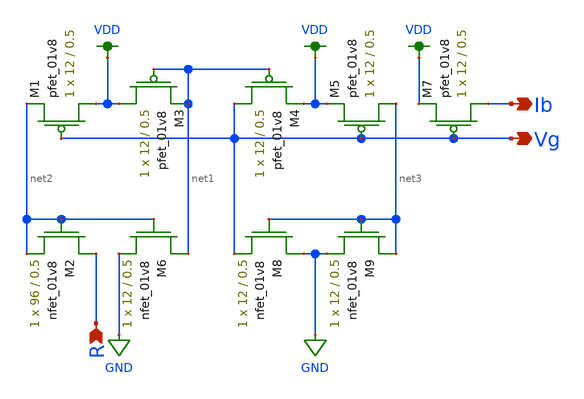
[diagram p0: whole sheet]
** sch_path: bias_gen.sch
**.subckt bias_gen R Ib Vg
*.ipin R
*.opin Ib
*.opin Vg
XM2 R net2 net2 GND sky130_fd_pr__nfet_01v8 L=0.5 W=96 nf=1 ad='int((nf+1)/2) * W/nf * 0.29' as='int((nf+2)/2) * W/nf * 0.29'
+ pd='2*int((nf+1)/2) * (W/nf + 0.29)' ps='2*int((nf+2)/2) * (W/nf + 0.29)' nrd='0.29 / W' nrs='0.29 / W'
+ sa=0 sb=0 sd=0 mult=1 m=1
XM3 VDD net1 net1 VDD sky130_fd_pr__pfet_01v8 L=0.5 W=12 nf=1 ad='int((nf+1)/2) * W/nf * 0.29' as='int((nf+2)/2) * W/nf * 0.29'
+ pd='2*int((nf+1)/2) * (W/nf + 0.29)' ps='2*int((nf+2)/2) * (W/nf + 0.29)' nrd='0.29 / W' nrs='0.29 / W'
+ sa=0 sb=0 sd=0 mult=1 m=1
XM1 VDD Vg net2 VDD sky130_fd_pr__pfet_01v8 L=0.5 W=12 nf=1 ad='int((nf+1)/2) * W/nf * 0.29' as='int((nf+2)/2) * W/nf * 0.29'
+ pd='2*int((nf+1)/2) * (W/nf + 0.29)' ps='2*int((nf+2)/2) * (W/nf + 0.29)' nrd='0.29 / W' nrs='0.29 / W'
+ sa=0 sb=0 sd=0 mult=1 m=1
XM4 Vg net1 VDD VDD sky130_fd_pr__pfet_01v8 L=0.5 W=12 nf=1 ad='int((nf+1)/2) * W/nf * 0.29' as='int((nf+2)/2) * W/nf * 0.29'
+ pd='2*int((nf+1)/2) * (W/nf + 0.29)' ps='2*int((nf+2)/2) * (W/nf + 0.29)' nrd='0.29 / W' nrs='0.29 / W'
+ sa=0 sb=0 sd=0 mult=1 m=1
XM5 net3 Vg VDD VDD sky130_fd_pr__pfet_01v8 L=0.5 W=12 nf=1 ad='int((nf+1)/2) * W/nf * 0.29' as='int((nf+2)/2) * W/nf * 0.29'
+ pd='2*int((nf+1)/2) * (W/nf + 0.29)' ps='2*int((nf+2)/2) * (W/nf + 0.29)' nrd='0.29 / W' nrs='0.29 / W'
+ sa=0 sb=0 sd=0 mult=1 m=1
XM7 Ib Vg VDD VDD sky130_fd_pr__pfet_01v8 L=0.5 W=12 nf=1 ad='int((nf+1)/2) * W/nf * 0.29' as='int((nf+2)/2) * W/nf * 0.29'
+ pd='2*int((nf+1)/2) * (W/nf + 0.29)' ps='2*int((nf+2)/2) * (W/nf + 0.29)' nrd='0.29 / W' nrs='0.29 / W'
+ sa=0 sb=0 sd=0 mult=1 m=1
XM6 net1 net2 GND GND sky130_fd_pr__nfet_01v8 L=0.5 W=12 nf=1 ad='int((nf+1)/2) * W/nf * 0.29' as='int((nf+2)/2) * W/nf * 0.29'
+ pd='2*int((nf+1)/2) * (W/nf + 0.29)' ps='2*int((nf+2)/2) * (W/nf + 0.29)' nrd='0.29 / W' nrs='0.29 / W'
+ sa=0 sb=0 sd=0 mult=1 m=1
XM8 GND net3 Vg GND sky130_fd_pr__nfet_01v8 L=0.5 W=12 nf=1 ad='int((nf+1)/2) * W/nf * 0.29' as='int((nf+2)/2) * W/nf * 0.29'
+ pd='2*int((nf+1)/2) * (W/nf + 0.29)' ps='2*int((nf+2)/2) * (W/nf + 0.29)' nrd='0.29 / W' nrs='0.29 / W'
+ sa=0 sb=0 sd=0 mult=1 m=1
XM9 net3 net3 GND GND sky130_fd_pr__nfet_01v8 L=0.5 W=12 nf=1 ad='int((nf+1)/2) * W/nf * 0.29' as='int((nf+2)/2) * W/nf * 0.29'
+ pd='2*int((nf+1)/2) * (W/nf + 0.29)' ps='2*int((nf+2)/2) * (W/nf + 0.29)' nrd='0.29 / W' nrs='0.29 / W'
+ sa=0 sb=0 sd=0 mult=1 m=1
**.ends
.GLOBAL VDD
.GLOBAL GND
.end
